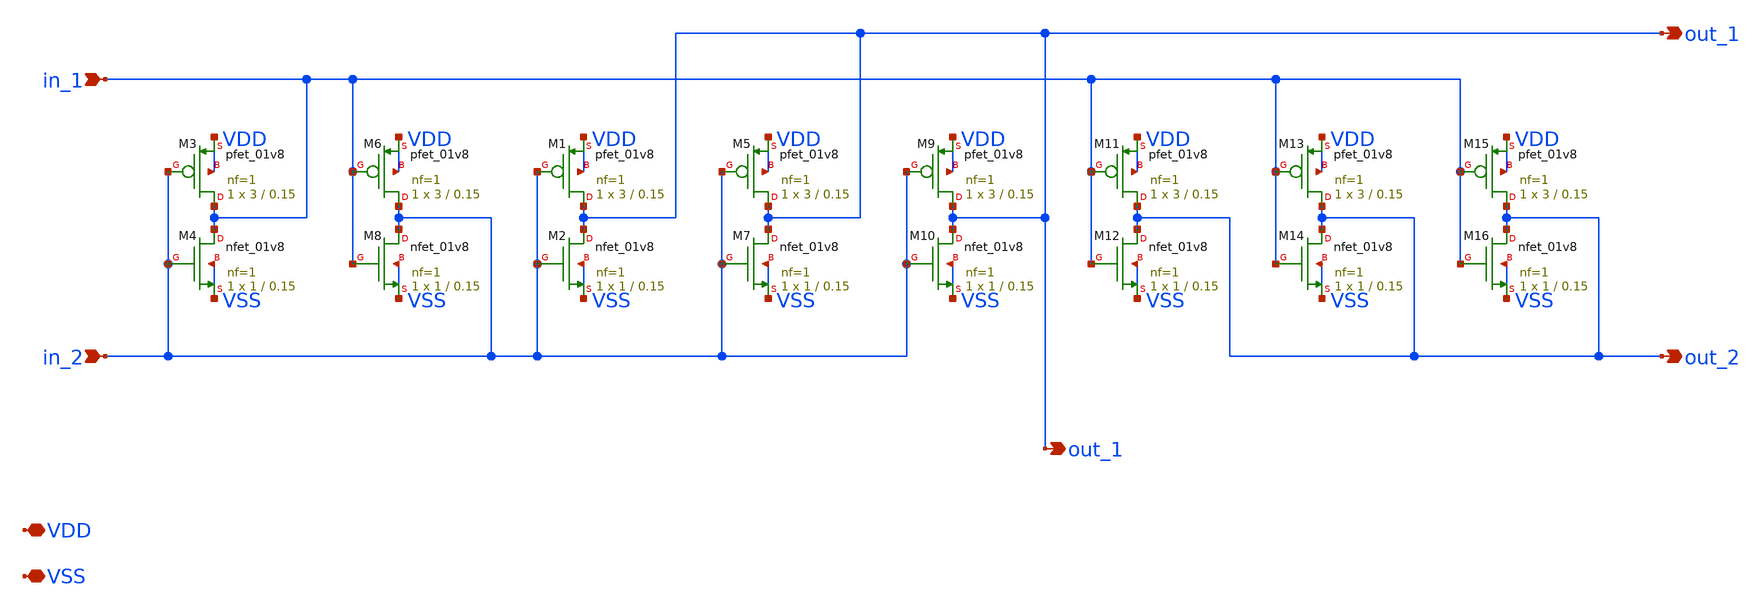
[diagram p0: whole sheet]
** sch_path: xschem/delay_unit_laydriv.sch
**.subckt delay_unit_laydriv VDD in_1 out_1 VSS in_2 out_2 out_1
*.iopin VDD
*.ipin in_1
*.opin out_1
*.iopin VSS
*.ipin in_2
*.opin out_2
*.opin out_1
XM3 in_1 in_2 VDD VDD sky130_fd_pr__pfet_01v8 L=0.15 W=3 nf=1 ad='int((nf+1)/2) * W/nf * 0.29' as='int((nf+2)/2) * W/nf * 0.29'
+ pd='2*int((nf+1)/2) * (W/nf + 0.29)' ps='2*int((nf+2)/2) * (W/nf + 0.29)' nrd='0.29 / W' nrs='0.29 / W'
+ sa=0 sb=0 sd=0 mult=1 m=1
XM4 in_1 in_2 VSS VSS sky130_fd_pr__nfet_01v8 L=0.15 W=1 nf=1 ad='int((nf+1)/2) * W/nf * 0.29' as='int((nf+2)/2) * W/nf * 0.29'
+ pd='2*int((nf+1)/2) * (W/nf + 0.29)' ps='2*int((nf+2)/2) * (W/nf + 0.29)' nrd='0.29 / W' nrs='0.29 / W'
+ sa=0 sb=0 sd=0 mult=1 m=1
XM6 in_2 in_1 VDD VDD sky130_fd_pr__pfet_01v8 L=0.15 W=3 nf=1 ad='int((nf+1)/2) * W/nf * 0.29' as='int((nf+2)/2) * W/nf * 0.29'
+ pd='2*int((nf+1)/2) * (W/nf + 0.29)' ps='2*int((nf+2)/2) * (W/nf + 0.29)' nrd='0.29 / W' nrs='0.29 / W'
+ sa=0 sb=0 sd=0 mult=1 m=1
XM8 in_2 in_1 VSS VSS sky130_fd_pr__nfet_01v8 L=0.15 W=1 nf=1 ad='int((nf+1)/2) * W/nf * 0.29' as='int((nf+2)/2) * W/nf * 0.29'
+ pd='2*int((nf+1)/2) * (W/nf + 0.29)' ps='2*int((nf+2)/2) * (W/nf + 0.29)' nrd='0.29 / W' nrs='0.29 / W'
+ sa=0 sb=0 sd=0 mult=1 m=1
XM1 out_1 in_2 VDD VDD sky130_fd_pr__pfet_01v8 L=0.15 W=3 nf=1 ad='int((nf+1)/2) * W/nf * 0.29' as='int((nf+2)/2) * W/nf * 0.29'
+ pd='2*int((nf+1)/2) * (W/nf + 0.29)' ps='2*int((nf+2)/2) * (W/nf + 0.29)' nrd='0.29 / W' nrs='0.29 / W'
+ sa=0 sb=0 sd=0 mult=1 m=1
XM2 out_1 in_2 VSS VSS sky130_fd_pr__nfet_01v8 L=0.15 W=1 nf=1 ad='int((nf+1)/2) * W/nf * 0.29' as='int((nf+2)/2) * W/nf * 0.29'
+ pd='2*int((nf+1)/2) * (W/nf + 0.29)' ps='2*int((nf+2)/2) * (W/nf + 0.29)' nrd='0.29 / W' nrs='0.29 / W'
+ sa=0 sb=0 sd=0 mult=1 m=1
XM5 out_1 in_2 VDD VDD sky130_fd_pr__pfet_01v8 L=0.15 W=3 nf=1 ad='int((nf+1)/2) * W/nf * 0.29' as='int((nf+2)/2) * W/nf * 0.29'
+ pd='2*int((nf+1)/2) * (W/nf + 0.29)' ps='2*int((nf+2)/2) * (W/nf + 0.29)' nrd='0.29 / W' nrs='0.29 / W'
+ sa=0 sb=0 sd=0 mult=1 m=1
XM7 out_1 in_2 VSS VSS sky130_fd_pr__nfet_01v8 L=0.15 W=1 nf=1 ad='int((nf+1)/2) * W/nf * 0.29' as='int((nf+2)/2) * W/nf * 0.29'
+ pd='2*int((nf+1)/2) * (W/nf + 0.29)' ps='2*int((nf+2)/2) * (W/nf + 0.29)' nrd='0.29 / W' nrs='0.29 / W'
+ sa=0 sb=0 sd=0 mult=1 m=1
XM9 out_1 in_2 VDD VDD sky130_fd_pr__pfet_01v8 L=0.15 W=3 nf=1 ad='int((nf+1)/2) * W/nf * 0.29' as='int((nf+2)/2) * W/nf * 0.29'
+ pd='2*int((nf+1)/2) * (W/nf + 0.29)' ps='2*int((nf+2)/2) * (W/nf + 0.29)' nrd='0.29 / W' nrs='0.29 / W'
+ sa=0 sb=0 sd=0 mult=1 m=1
XM10 out_1 in_2 VSS VSS sky130_fd_pr__nfet_01v8 L=0.15 W=1 nf=1 ad='int((nf+1)/2) * W/nf * 0.29' as='int((nf+2)/2) * W/nf * 0.29'
+ pd='2*int((nf+1)/2) * (W/nf + 0.29)' ps='2*int((nf+2)/2) * (W/nf + 0.29)' nrd='0.29 / W' nrs='0.29 / W'
+ sa=0 sb=0 sd=0 mult=1 m=1
XM11 out_2 in_1 VDD VDD sky130_fd_pr__pfet_01v8 L=0.15 W=3 nf=1 ad='int((nf+1)/2) * W/nf * 0.29' as='int((nf+2)/2) * W/nf * 0.29'
+ pd='2*int((nf+1)/2) * (W/nf + 0.29)' ps='2*int((nf+2)/2) * (W/nf + 0.29)' nrd='0.29 / W' nrs='0.29 / W'
+ sa=0 sb=0 sd=0 mult=1 m=1
XM12 out_2 in_1 VSS VSS sky130_fd_pr__nfet_01v8 L=0.15 W=1 nf=1 ad='int((nf+1)/2) * W/nf * 0.29' as='int((nf+2)/2) * W/nf * 0.29'
+ pd='2*int((nf+1)/2) * (W/nf + 0.29)' ps='2*int((nf+2)/2) * (W/nf + 0.29)' nrd='0.29 / W' nrs='0.29 / W'
+ sa=0 sb=0 sd=0 mult=1 m=1
XM13 out_2 in_1 VDD VDD sky130_fd_pr__pfet_01v8 L=0.15 W=3 nf=1 ad='int((nf+1)/2) * W/nf * 0.29' as='int((nf+2)/2) * W/nf * 0.29'
+ pd='2*int((nf+1)/2) * (W/nf + 0.29)' ps='2*int((nf+2)/2) * (W/nf + 0.29)' nrd='0.29 / W' nrs='0.29 / W'
+ sa=0 sb=0 sd=0 mult=1 m=1
XM14 out_2 in_1 VSS VSS sky130_fd_pr__nfet_01v8 L=0.15 W=1 nf=1 ad='int((nf+1)/2) * W/nf * 0.29' as='int((nf+2)/2) * W/nf * 0.29'
+ pd='2*int((nf+1)/2) * (W/nf + 0.29)' ps='2*int((nf+2)/2) * (W/nf + 0.29)' nrd='0.29 / W' nrs='0.29 / W'
+ sa=0 sb=0 sd=0 mult=1 m=1
XM15 out_2 in_1 VDD VDD sky130_fd_pr__pfet_01v8 L=0.15 W=3 nf=1 ad='int((nf+1)/2) * W/nf * 0.29' as='int((nf+2)/2) * W/nf * 0.29'
+ pd='2*int((nf+1)/2) * (W/nf + 0.29)' ps='2*int((nf+2)/2) * (W/nf + 0.29)' nrd='0.29 / W' nrs='0.29 / W'
+ sa=0 sb=0 sd=0 mult=1 m=1
XM16 out_2 in_1 VSS VSS sky130_fd_pr__nfet_01v8 L=0.15 W=1 nf=1 ad='int((nf+1)/2) * W/nf * 0.29' as='int((nf+2)/2) * W/nf * 0.29'
+ pd='2*int((nf+1)/2) * (W/nf + 0.29)' ps='2*int((nf+2)/2) * (W/nf + 0.29)' nrd='0.29 / W' nrs='0.29 / W'
+ sa=0 sb=0 sd=0 mult=1 m=1
**.ends
.end
